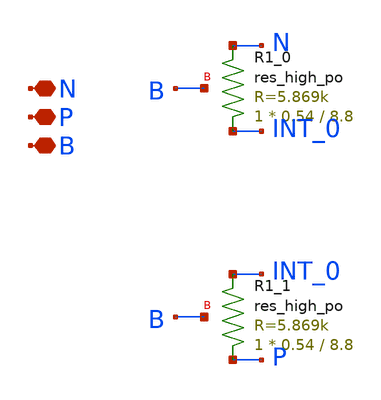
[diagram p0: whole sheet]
** sch_path: ip/sun_tr_sky130nm/design/SUN_TR_SKY130NM/SUNTR_RES12.sch
**.subckt SUNTR_RES12 N P B
*.iopin N
*.iopin P
*.iopin B
XR1_0 INT_0 N B sky130_fd_pr__res_high_po W=0.54 L=8.8 mult=1 m=1
XR1_1 P INT_0 B sky130_fd_pr__res_high_po W=0.54 L=8.8 mult=1 m=1
**.ends
.end
